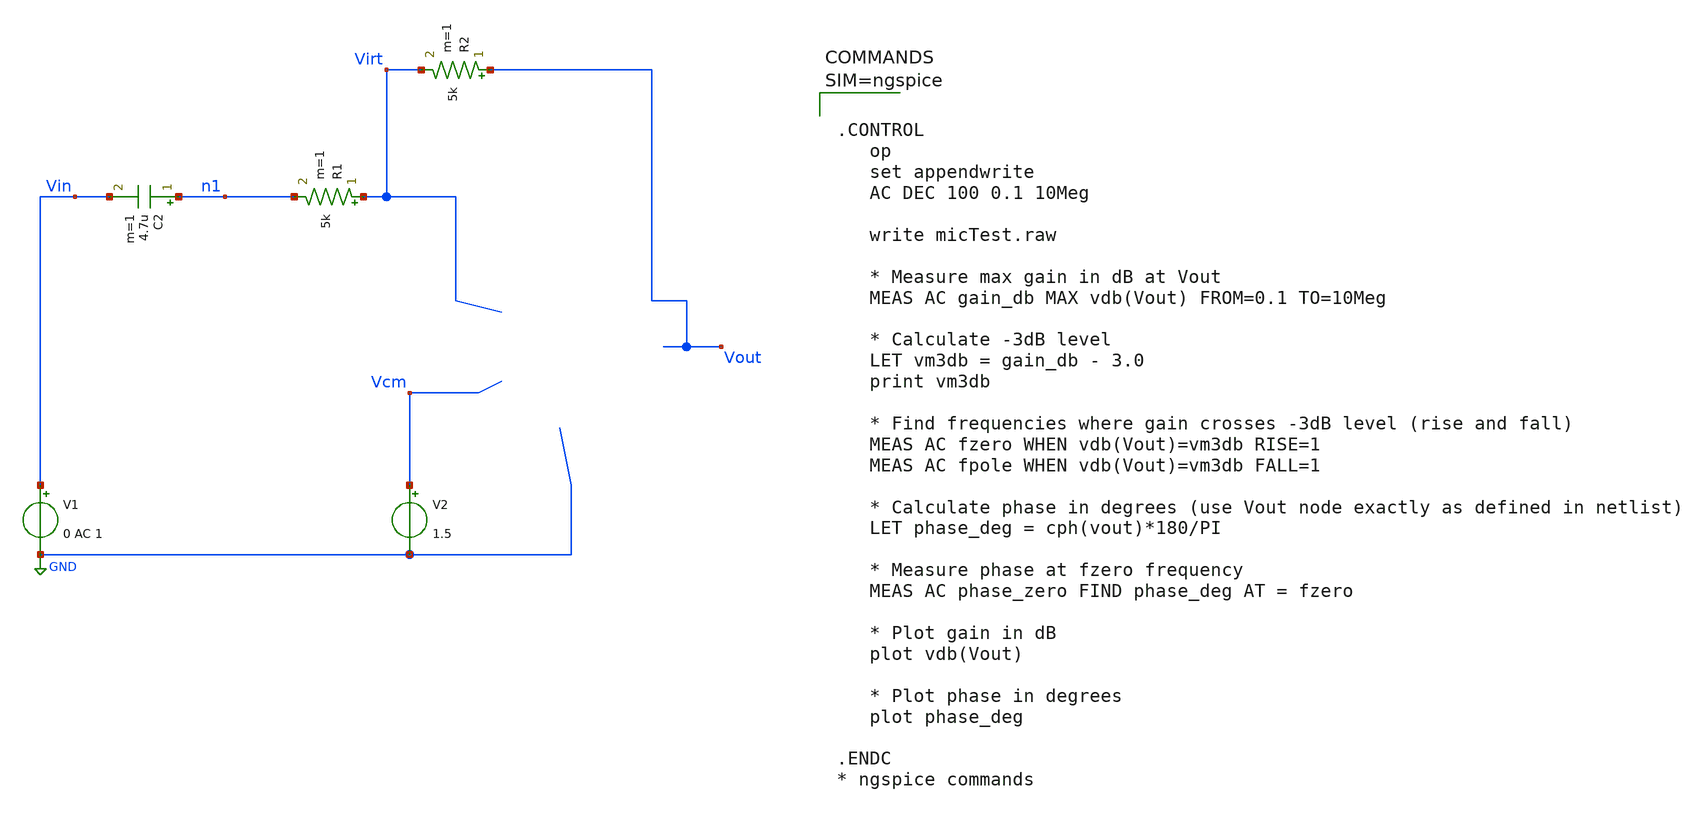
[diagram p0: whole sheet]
** sch_path: xschem/untitled-3.sch
**.subckt untitled-3
V1 Vin GND 0 AC 1
R1 Virt n1 5k m=1
C2 n1 Vin 4.7u m=1
R2 Vout Virt 5k m=1
V2 Vcm GND 1.5
**** begin user architecture code



.CONTROL
   op
   set appendwrite
   AC DEC 100 0.1 10Meg

   write micTest.raw

   * Measure max gain in dB at Vout
   MEAS AC gain_db MAX vdb(Vout) FROM=0.1 TO=10Meg

   * Calculate -3dB level
   LET vm3db = gain_db - 3.0
   print vm3db

   * Find frequencies where gain crosses -3dB level (rise and fall)
   MEAS AC fzero WHEN vdb(Vout)=vm3db RISE=1
   MEAS AC fpole WHEN vdb(Vout)=vm3db FALL=1

   * Calculate phase in degrees (use Vout node exactly as defined in netlist)
   LET phase_deg = cph(vout)*180/PI

   * Measure phase at fzero frequency
   MEAS AC phase_zero FIND phase_deg AT = fzero

   * Plot gain in dB
   plot vdb(Vout)

   * Plot phase in degrees
   plot phase_deg

.ENDC
* ngspice commands


**** end user architecture code
**.ends
.GLOBAL GND
.end
